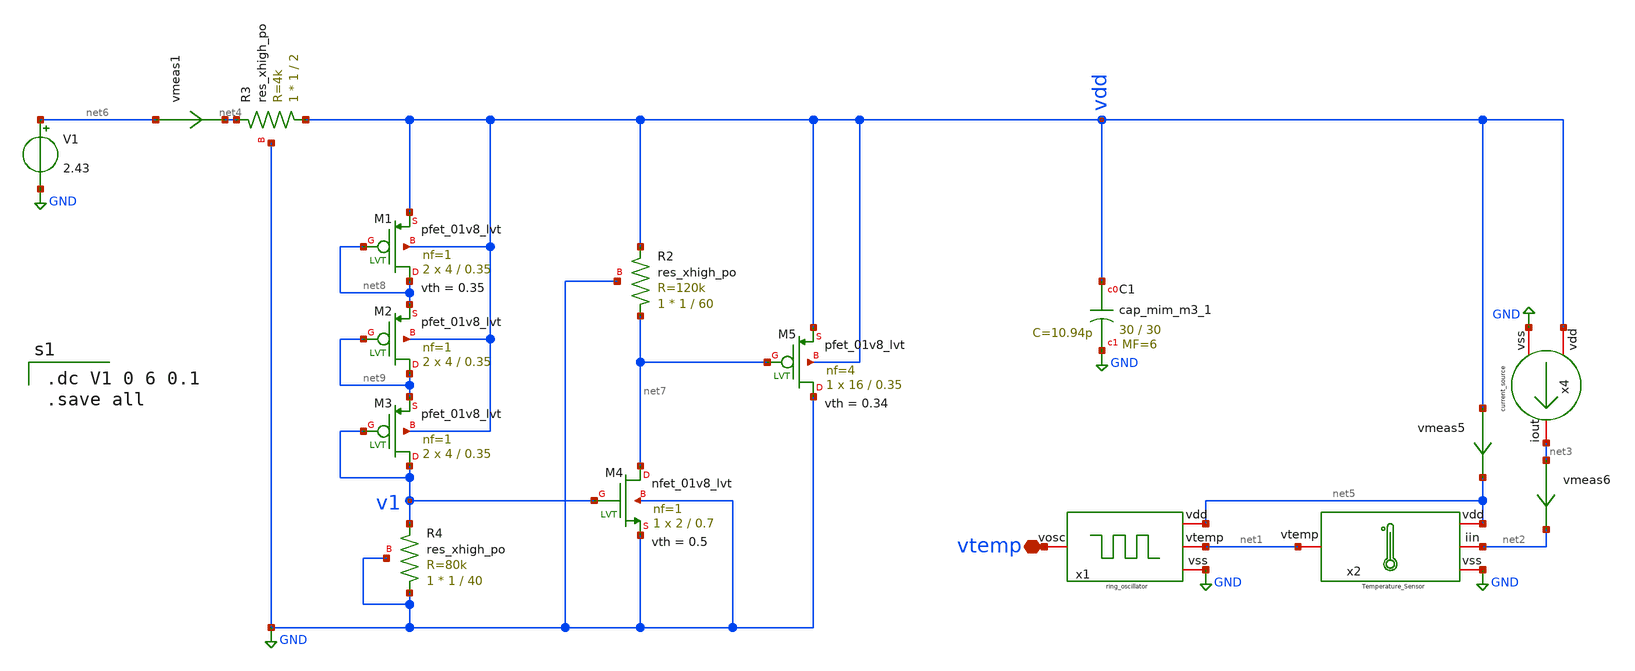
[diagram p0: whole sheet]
** sch_path: XSCHEM/prueba_vlim_now.sch
**.subckt prueba_vlim_now vtemp
*.iopin vtemp
vmeas6 net3 net2 0
.save i(vmeas6)
vmeas1 net6 net4 0
.save i(vmeas1)
vmeas5 vdd net5 0
.save i(vmeas5)
XC1 vdd GND sky130_fd_pr__cap_mim_m3_1 W=30 L=30 MF=6 m=6
x2 net5 net1 net2 GND Temperature_Sensor
x4 vdd net3 GND current_source
V1 net6 GND 2.43
x1 net5 vtemp GND net1 ring_oscillator
XM4 net7 v1 GND GND sky130_fd_pr__nfet_01v8_lvt L=0.7 W=2 nf=1 ad='int((nf+1)/2) * W/nf * 0.29' as='int((nf+2)/2) * W/nf * 0.29'
+ pd='2*int((nf+1)/2) * (W/nf + 0.29)' ps='2*int((nf+2)/2) * (W/nf + 0.29)' nrd='0.29 / W' nrs='0.29 / W'
+ sa=0 sb=0 sd=0 mult=1 m=1
XM5 GND net7 vdd vdd sky130_fd_pr__pfet_01v8_lvt L=0.35 W=16 nf=4 ad='int((nf+1)/2) * W/nf * 0.29' as='int((nf+2)/2) * W/nf * 0.29'
+ pd='2*int((nf+1)/2) * (W/nf + 0.29)' ps='2*int((nf+2)/2) * (W/nf + 0.29)' nrd='0.29 / W' nrs='0.29 / W'
+ sa=0 sb=0 sd=0 mult=1 m=1
XM1 net8 net8 vdd vdd sky130_fd_pr__pfet_01v8_lvt L=0.35 W=4 nf=1 ad='int((nf+1)/2) * W/nf * 0.29' as='int((nf+2)/2) * W/nf * 0.29'
+ pd='2*int((nf+1)/2) * (W/nf + 0.29)' ps='2*int((nf+2)/2) * (W/nf + 0.29)' nrd='0.29 / W' nrs='0.29 / W'
+ sa=0 sb=0 sd=0 mult=2 m=2
XM2 net9 net9 net8 vdd sky130_fd_pr__pfet_01v8_lvt L=0.35 W=4 nf=1 ad='int((nf+1)/2) * W/nf * 0.29' as='int((nf+2)/2) * W/nf * 0.29'
+ pd='2*int((nf+1)/2) * (W/nf + 0.29)' ps='2*int((nf+2)/2) * (W/nf + 0.29)' nrd='0.29 / W' nrs='0.29 / W'
+ sa=0 sb=0 sd=0 mult=2 m=2
XM3 v1 v1 net9 vdd sky130_fd_pr__pfet_01v8_lvt L=0.35 W=4 nf=1 ad='int((nf+1)/2) * W/nf * 0.29' as='int((nf+2)/2) * W/nf * 0.29'
+ pd='2*int((nf+1)/2) * (W/nf + 0.29)' ps='2*int((nf+2)/2) * (W/nf + 0.29)' nrd='0.29 / W' nrs='0.29 / W'
+ sa=0 sb=0 sd=0 mult=2 m=2
XR3 vdd net4 GND sky130_fd_pr__res_xhigh_po W=1 L=2 mult=1 m=1
XR2 net7 vdd GND sky130_fd_pr__res_xhigh_po W=1 L=60 mult=1 m=1
XR4 GND v1 GND sky130_fd_pr__res_xhigh_po W=1 L=40 mult=1 m=1
**** begin user architecture code

.dc V1 0 6 0.1
.save all


** opencircuitdesign pdks install
.lib $::SKYWATER_MODELS/sky130.lib.spice tt


**** end user architecture code
**.ends
.GLOBAL GND
.end
